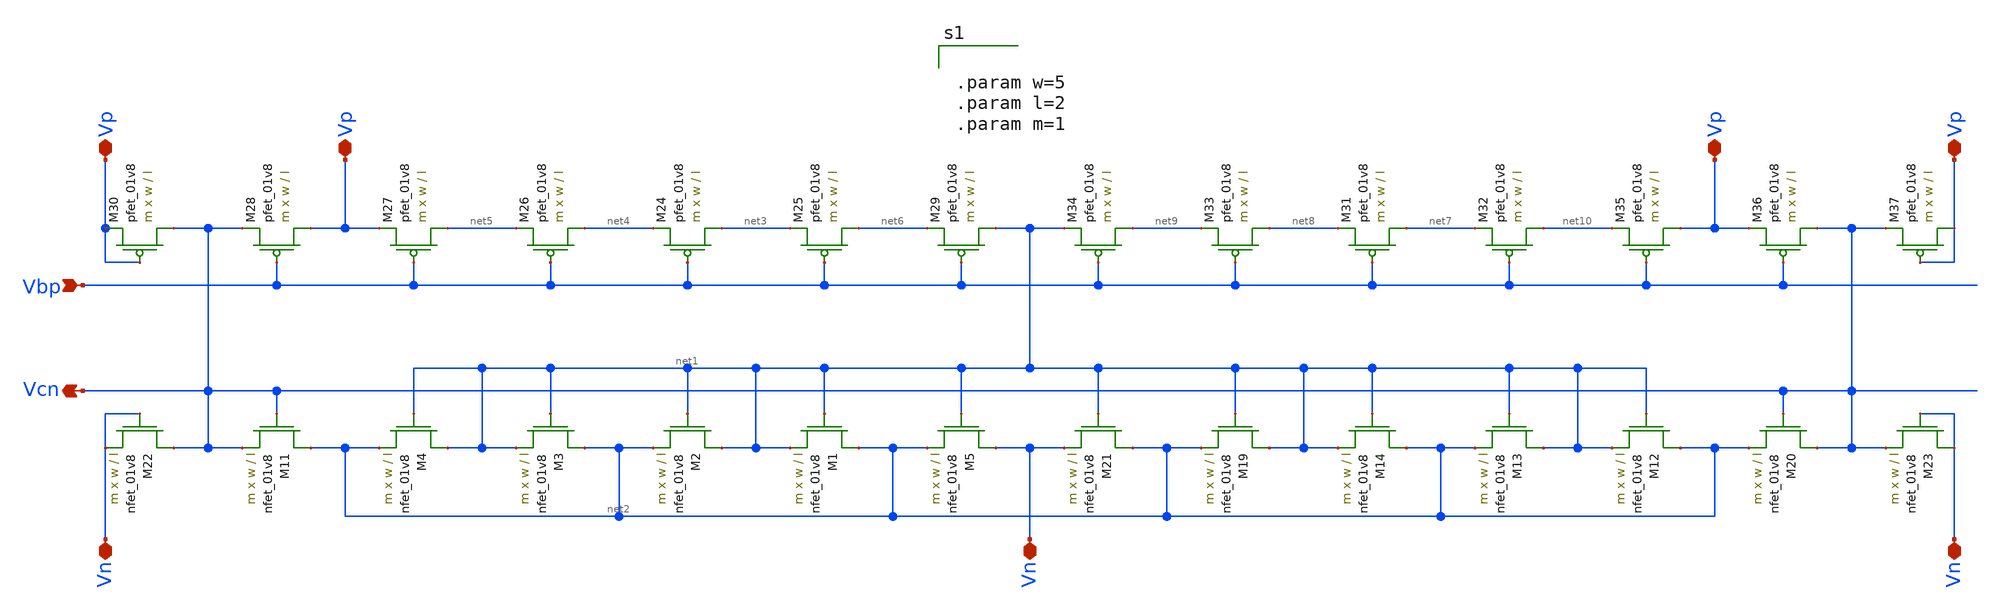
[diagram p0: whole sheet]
** sch_path: schematic/cascode_generator_LDS.sch
**.subckt cascode_generator_LDS Vn Vcn Vn Vn Vp Vp Vbp Vp Vp
*.iopin Vn
*.opin Vcn
*.iopin Vn
*.iopin Vn
*.iopin Vp
*.iopin Vp
*.ipin Vbp
*.iopin Vp
*.iopin Vp
XM1 net2 net1 net1 GND sky130_fd_pr__nfet_01v8 L=l W=w nf=1 ad='int((nf+1)/2) * W/nf * 0.29' as='int((nf+2)/2) * W/nf * 0.29'
+ pd='2*int((nf+1)/2) * (W/nf + 0.29)' ps='2*int((nf+2)/2) * (W/nf + 0.29)' nrd='0.29 / W' nrs='0.29 / W'
+ sa=0 sb=0 sd=0 mult=m m=m
XM2 net1 net1 net2 GND sky130_fd_pr__nfet_01v8 L=l W=w nf=1 ad='int((nf+1)/2) * W/nf * 0.29' as='int((nf+2)/2) * W/nf * 0.29'
+ pd='2*int((nf+1)/2) * (W/nf + 0.29)' ps='2*int((nf+2)/2) * (W/nf + 0.29)' nrd='0.29 / W' nrs='0.29 / W'
+ sa=0 sb=0 sd=0 mult=m m=m
XM3 net2 net1 net1 GND sky130_fd_pr__nfet_01v8 L=l W=w nf=1 ad='int((nf+1)/2) * W/nf * 0.29' as='int((nf+2)/2) * W/nf * 0.29'
+ pd='2*int((nf+1)/2) * (W/nf + 0.29)' ps='2*int((nf+2)/2) * (W/nf + 0.29)' nrd='0.29 / W' nrs='0.29 / W'
+ sa=0 sb=0 sd=0 mult=m m=m
XM4 net1 net1 net2 GND sky130_fd_pr__nfet_01v8 L=l W=w nf=1 ad='int((nf+1)/2) * W/nf * 0.29' as='int((nf+2)/2) * W/nf * 0.29'
+ pd='2*int((nf+1)/2) * (W/nf + 0.29)' ps='2*int((nf+2)/2) * (W/nf + 0.29)' nrd='0.29 / W' nrs='0.29 / W'
+ sa=0 sb=0 sd=0 mult=m m=m
XM5 Vn net1 net2 GND sky130_fd_pr__nfet_01v8 L=l W=w nf=1 ad='int((nf+1)/2) * W/nf * 0.29' as='int((nf+2)/2) * W/nf * 0.29'
+ pd='2*int((nf+1)/2) * (W/nf + 0.29)' ps='2*int((nf+2)/2) * (W/nf + 0.29)' nrd='0.29 / W' nrs='0.29 / W'
+ sa=0 sb=0 sd=0 mult=m m=m
XM11 net2 Vcn Vcn GND sky130_fd_pr__nfet_01v8 L=l W=w nf=1 ad='int((nf+1)/2) * W/nf * 0.29' as='int((nf+2)/2) * W/nf * 0.29'
+ pd='2*int((nf+1)/2) * (W/nf + 0.29)' ps='2*int((nf+2)/2) * (W/nf + 0.29)' nrd='0.29 / W' nrs='0.29 / W'
+ sa=0 sb=0 sd=0 mult=m m=m
XM12 net2 net1 net1 GND sky130_fd_pr__nfet_01v8 L=l W=w nf=1 ad='int((nf+1)/2) * W/nf * 0.29' as='int((nf+2)/2) * W/nf * 0.29'
+ pd='2*int((nf+1)/2) * (W/nf + 0.29)' ps='2*int((nf+2)/2) * (W/nf + 0.29)' nrd='0.29 / W' nrs='0.29 / W'
+ sa=0 sb=0 sd=0 mult=m m=m
XM13 net1 net1 net2 GND sky130_fd_pr__nfet_01v8 L=l W=w nf=1 ad='int((nf+1)/2) * W/nf * 0.29' as='int((nf+2)/2) * W/nf * 0.29'
+ pd='2*int((nf+1)/2) * (W/nf + 0.29)' ps='2*int((nf+2)/2) * (W/nf + 0.29)' nrd='0.29 / W' nrs='0.29 / W'
+ sa=0 sb=0 sd=0 mult=m m=m
XM14 net2 net1 net1 GND sky130_fd_pr__nfet_01v8 L=l W=w nf=1 ad='int((nf+1)/2) * W/nf * 0.29' as='int((nf+2)/2) * W/nf * 0.29'
+ pd='2*int((nf+1)/2) * (W/nf + 0.29)' ps='2*int((nf+2)/2) * (W/nf + 0.29)' nrd='0.29 / W' nrs='0.29 / W'
+ sa=0 sb=0 sd=0 mult=m m=m
XM19 net1 net1 net2 GND sky130_fd_pr__nfet_01v8 L=l W=w nf=1 ad='int((nf+1)/2) * W/nf * 0.29' as='int((nf+2)/2) * W/nf * 0.29'
+ pd='2*int((nf+1)/2) * (W/nf + 0.29)' ps='2*int((nf+2)/2) * (W/nf + 0.29)' nrd='0.29 / W' nrs='0.29 / W'
+ sa=0 sb=0 sd=0 mult=m m=m
XM20 Vcn Vcn net2 GND sky130_fd_pr__nfet_01v8 L=l W=w nf=1 ad='int((nf+1)/2) * W/nf * 0.29' as='int((nf+2)/2) * W/nf * 0.29'
+ pd='2*int((nf+1)/2) * (W/nf + 0.29)' ps='2*int((nf+2)/2) * (W/nf + 0.29)' nrd='0.29 / W' nrs='0.29 / W'
+ sa=0 sb=0 sd=0 mult=m m=m
XM21 net2 net1 Vn GND sky130_fd_pr__nfet_01v8 L=l W=w nf=1 ad='int((nf+1)/2) * W/nf * 0.29' as='int((nf+2)/2) * W/nf * 0.29'
+ pd='2*int((nf+1)/2) * (W/nf + 0.29)' ps='2*int((nf+2)/2) * (W/nf + 0.29)' nrd='0.29 / W' nrs='0.29 / W'
+ sa=0 sb=0 sd=0 mult=m m=m
XM22 Vcn Vn Vn GND sky130_fd_pr__nfet_01v8 L=l W=w nf=1 ad='int((nf+1)/2) * W/nf * 0.29' as='int((nf+2)/2) * W/nf * 0.29'
+ pd='2*int((nf+1)/2) * (W/nf + 0.29)' ps='2*int((nf+2)/2) * (W/nf + 0.29)' nrd='0.29 / W' nrs='0.29 / W'
+ sa=0 sb=0 sd=0 mult=m m=m
XM23 Vn Vn Vcn GND sky130_fd_pr__nfet_01v8 L=l W=w nf=1 ad='int((nf+1)/2) * W/nf * 0.29' as='int((nf+2)/2) * W/nf * 0.29'
+ pd='2*int((nf+1)/2) * (W/nf + 0.29)' ps='2*int((nf+2)/2) * (W/nf + 0.29)' nrd='0.29 / W' nrs='0.29 / W'
+ sa=0 sb=0 sd=0 mult=m m=m
XM24 net3 Vbp net4 VDD sky130_fd_pr__pfet_01v8 L=l W=w nf=1 ad='int((nf+1)/2) * W/nf * 0.29' as='int((nf+2)/2) * W/nf * 0.29'
+ pd='2*int((nf+1)/2) * (W/nf + 0.29)' ps='2*int((nf+2)/2) * (W/nf + 0.29)' nrd='0.29 / W' nrs='0.29 / W'
+ sa=0 sb=0 sd=0 mult=m m=m
XM25 net6 Vbp net3 VDD sky130_fd_pr__pfet_01v8 L=l W=w nf=1 ad='int((nf+1)/2) * W/nf * 0.29' as='int((nf+2)/2) * W/nf * 0.29'
+ pd='2*int((nf+1)/2) * (W/nf + 0.29)' ps='2*int((nf+2)/2) * (W/nf + 0.29)' nrd='0.29 / W' nrs='0.29 / W'
+ sa=0 sb=0 sd=0 mult=m m=m
XM26 net4 Vbp net5 VDD sky130_fd_pr__pfet_01v8 L=l W=w nf=1 ad='int((nf+1)/2) * W/nf * 0.29' as='int((nf+2)/2) * W/nf * 0.29'
+ pd='2*int((nf+1)/2) * (W/nf + 0.29)' ps='2*int((nf+2)/2) * (W/nf + 0.29)' nrd='0.29 / W' nrs='0.29 / W'
+ sa=0 sb=0 sd=0 mult=m m=m
XM27 net5 Vbp Vp VDD sky130_fd_pr__pfet_01v8 L=l W=w nf=1 ad='int((nf+1)/2) * W/nf * 0.29' as='int((nf+2)/2) * W/nf * 0.29'
+ pd='2*int((nf+1)/2) * (W/nf + 0.29)' ps='2*int((nf+2)/2) * (W/nf + 0.29)' nrd='0.29 / W' nrs='0.29 / W'
+ sa=0 sb=0 sd=0 mult=m m=m
XM28 Vp Vbp Vcn VDD sky130_fd_pr__pfet_01v8 L=l W=w nf=1 ad='int((nf+1)/2) * W/nf * 0.29' as='int((nf+2)/2) * W/nf * 0.29'
+ pd='2*int((nf+1)/2) * (W/nf + 0.29)' ps='2*int((nf+2)/2) * (W/nf + 0.29)' nrd='0.29 / W' nrs='0.29 / W'
+ sa=0 sb=0 sd=0 mult=m m=m
XM29 net1 Vbp net6 VDD sky130_fd_pr__pfet_01v8 L=l W=w nf=1 ad='int((nf+1)/2) * W/nf * 0.29' as='int((nf+2)/2) * W/nf * 0.29'
+ pd='2*int((nf+1)/2) * (W/nf + 0.29)' ps='2*int((nf+2)/2) * (W/nf + 0.29)' nrd='0.29 / W' nrs='0.29 / W'
+ sa=0 sb=0 sd=0 mult=m m=m
XM30 Vcn Vp Vp VDD sky130_fd_pr__pfet_01v8 L=l W=w nf=1 ad='int((nf+1)/2) * W/nf * 0.29' as='int((nf+2)/2) * W/nf * 0.29'
+ pd='2*int((nf+1)/2) * (W/nf + 0.29)' ps='2*int((nf+2)/2) * (W/nf + 0.29)' nrd='0.29 / W' nrs='0.29 / W'
+ sa=0 sb=0 sd=0 mult=m m=m
XM31 net7 Vbp net8 VDD sky130_fd_pr__pfet_01v8 L=l W=w nf=1 ad='int((nf+1)/2) * W/nf * 0.29' as='int((nf+2)/2) * W/nf * 0.29'
+ pd='2*int((nf+1)/2) * (W/nf + 0.29)' ps='2*int((nf+2)/2) * (W/nf + 0.29)' nrd='0.29 / W' nrs='0.29 / W'
+ sa=0 sb=0 sd=0 mult=m m=m
XM32 net10 Vbp net7 VDD sky130_fd_pr__pfet_01v8 L=l W=w nf=1 ad='int((nf+1)/2) * W/nf * 0.29' as='int((nf+2)/2) * W/nf * 0.29'
+ pd='2*int((nf+1)/2) * (W/nf + 0.29)' ps='2*int((nf+2)/2) * (W/nf + 0.29)' nrd='0.29 / W' nrs='0.29 / W'
+ sa=0 sb=0 sd=0 mult=m m=m
XM33 net8 Vbp net9 VDD sky130_fd_pr__pfet_01v8 L=l W=w nf=1 ad='int((nf+1)/2) * W/nf * 0.29' as='int((nf+2)/2) * W/nf * 0.29'
+ pd='2*int((nf+1)/2) * (W/nf + 0.29)' ps='2*int((nf+2)/2) * (W/nf + 0.29)' nrd='0.29 / W' nrs='0.29 / W'
+ sa=0 sb=0 sd=0 mult=m m=m
XM34 net9 Vbp net1 VDD sky130_fd_pr__pfet_01v8 L=l W=w nf=1 ad='int((nf+1)/2) * W/nf * 0.29' as='int((nf+2)/2) * W/nf * 0.29'
+ pd='2*int((nf+1)/2) * (W/nf + 0.29)' ps='2*int((nf+2)/2) * (W/nf + 0.29)' nrd='0.29 / W' nrs='0.29 / W'
+ sa=0 sb=0 sd=0 mult=m m=m
XM35 Vp Vbp net10 VDD sky130_fd_pr__pfet_01v8 L=l W=w nf=1 ad='int((nf+1)/2) * W/nf * 0.29' as='int((nf+2)/2) * W/nf * 0.29'
+ pd='2*int((nf+1)/2) * (W/nf + 0.29)' ps='2*int((nf+2)/2) * (W/nf + 0.29)' nrd='0.29 / W' nrs='0.29 / W'
+ sa=0 sb=0 sd=0 mult=m m=m
XM36 Vcn Vbp Vp VDD sky130_fd_pr__pfet_01v8 L=l W=w nf=1 ad='int((nf+1)/2) * W/nf * 0.29' as='int((nf+2)/2) * W/nf * 0.29'
+ pd='2*int((nf+1)/2) * (W/nf + 0.29)' ps='2*int((nf+2)/2) * (W/nf + 0.29)' nrd='0.29 / W' nrs='0.29 / W'
+ sa=0 sb=0 sd=0 mult=m m=m
XM37 Vp Vp Vcn VDD sky130_fd_pr__pfet_01v8 L=l W=w nf=1 ad='int((nf+1)/2) * W/nf * 0.29' as='int((nf+2)/2) * W/nf * 0.29'
+ pd='2*int((nf+1)/2) * (W/nf + 0.29)' ps='2*int((nf+2)/2) * (W/nf + 0.29)' nrd='0.29 / W' nrs='0.29 / W'
+ sa=0 sb=0 sd=0 mult=m m=m
**** begin user architecture code


.param w=5
.param l=2
.param m=1


**** end user architecture code
**.ends
.end
